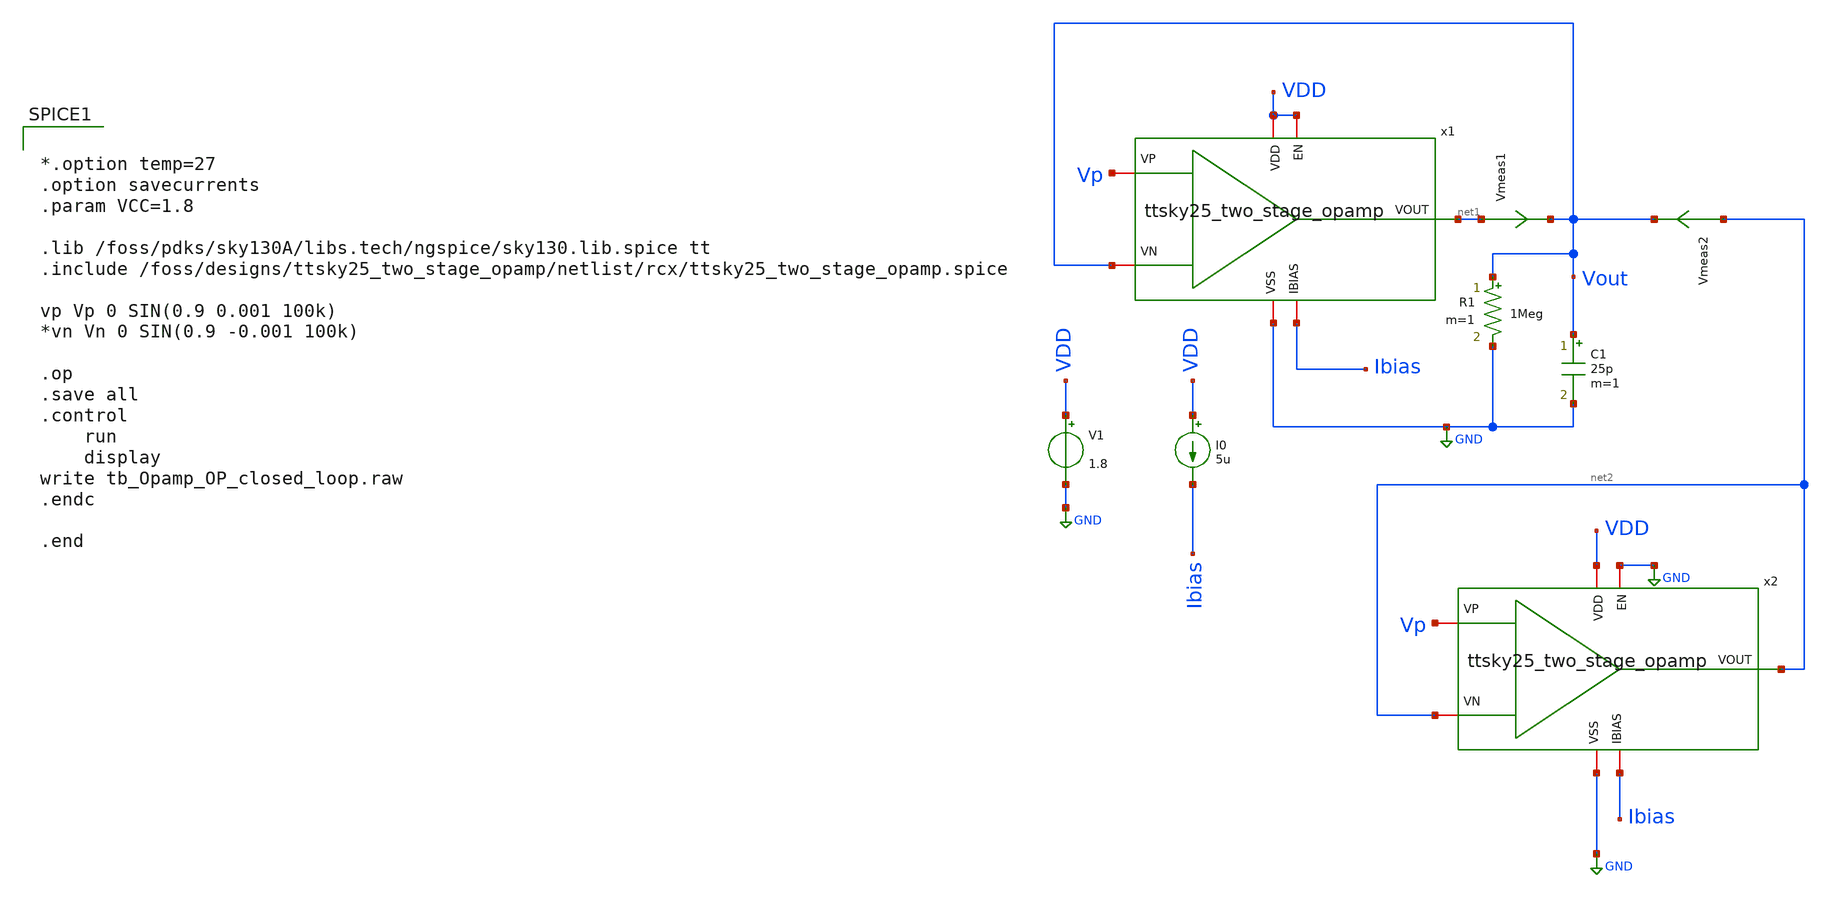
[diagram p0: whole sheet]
** sch_path: xschem/post-layout/testbenches/tb_Opamp_OP_closed_loop.sch
**.subckt tb_Opamp_OP_closed_loop
V1 VDD GND 1.8
I0 VDD Ibias 5u
C1 Vout GND 25p m=1
x1 VDD Ibias net1 Vout Vp VDD GND ttsky25_two_stage_opamp
Vmeas1 net1 Vout 0
.save i(vmeas1)
R1 Vout GND 1Meg m=1
x2 VDD Ibias net2 net2 Vp GND GND ttsky25_two_stage_opamp
Vmeas2 net2 Vout 0
.save i(vmeas2)
**** begin user architecture code


*.option temp=27
.option savecurrents
.param VCC=1.8

.lib /foss/pdks/sky130A/libs.tech/ngspice/sky130.lib.spice tt
.include /foss/designs/ttsky25_two_stage_opamp/netlist/rcx/ttsky25_two_stage_opamp.spice

vp Vp 0 SIN(0.9 0.001 100k)
*vn Vn 0 SIN(0.9 -0.001 100k)

.op
.save all
.control
	run
	display
write tb_Opamp_OP_closed_loop.raw
.endc

.end


**** end user architecture code
**.ends
.GLOBAL GND
.end
